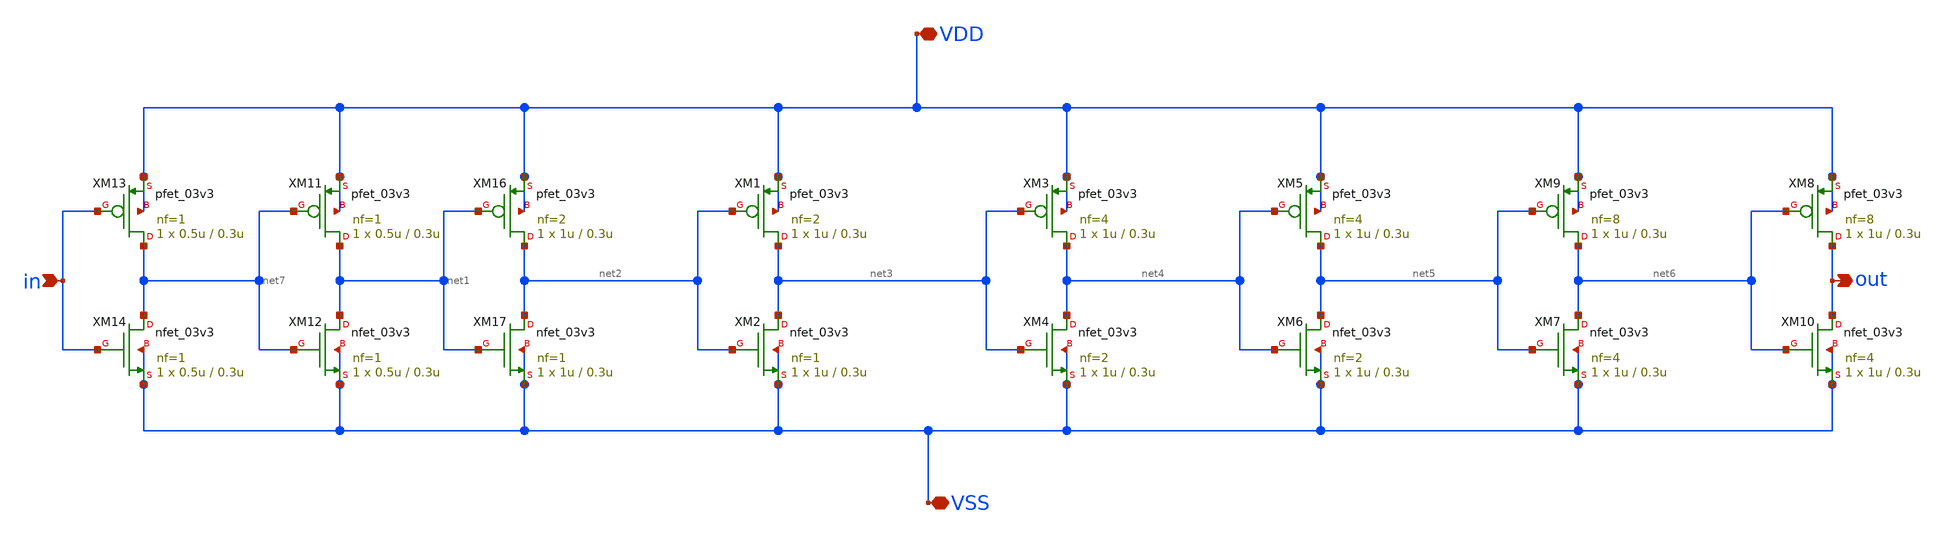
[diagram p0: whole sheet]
** sch_path: designs/libs/core_vco/vco_buffer/vco_buffer.sch
**.subckt vco_buffer in VDD VSS out
*.ipin in
*.iopin VDD
*.iopin VSS
*.opin out
XM16 net2 net1 VDD VDD pfet_03v3 L=0.3u W=1u nf=2 ad='int((nf+1)/2) * W/nf * 0.18u' as='int((nf+2)/2) * W/nf * 0.18u'
+ pd='2*int((nf+1)/2) * (W/nf + 0.18u)' ps='2*int((nf+2)/2) * (W/nf + 0.18u)' nrd='0.18u / W' nrs='0.18u / W'
+ sa=0 sb=0 sd=0 m=1
XM17 net2 net1 VSS VSS nfet_03v3 L=0.3u W=1u nf=1 ad='int((nf+1)/2) * W/nf * 0.18u' as='int((nf+2)/2) * W/nf * 0.18u'
+ pd='2*int((nf+1)/2) * (W/nf + 0.18u)' ps='2*int((nf+2)/2) * (W/nf + 0.18u)' nrd='0.18u / W' nrs='0.18u / W'
+ sa=0 sb=0 sd=0 m=1
XM2 net3 net2 VSS VSS nfet_03v3 L=0.3u W=1u nf=1 ad='int((nf+1)/2) * W/nf * 0.18u' as='int((nf+2)/2) * W/nf * 0.18u'
+ pd='2*int((nf+1)/2) * (W/nf + 0.18u)' ps='2*int((nf+2)/2) * (W/nf + 0.18u)' nrd='0.18u / W' nrs='0.18u / W'
+ sa=0 sb=0 sd=0 m=1
XM4 net4 net3 VSS VSS nfet_03v3 L=0.3u W=1u nf=2 ad='int((nf+1)/2) * W/nf * 0.18u' as='int((nf+2)/2) * W/nf * 0.18u'
+ pd='2*int((nf+1)/2) * (W/nf + 0.18u)' ps='2*int((nf+2)/2) * (W/nf + 0.18u)' nrd='0.18u / W' nrs='0.18u / W'
+ sa=0 sb=0 sd=0 m=1
XM6 net5 net4 VSS VSS nfet_03v3 L=0.3u W=1u nf=2 ad='int((nf+1)/2) * W/nf * 0.18u' as='int((nf+2)/2) * W/nf * 0.18u'
+ pd='2*int((nf+1)/2) * (W/nf + 0.18u)' ps='2*int((nf+2)/2) * (W/nf + 0.18u)' nrd='0.18u / W' nrs='0.18u / W'
+ sa=0 sb=0 sd=0 m=1
XM1 net3 net2 VDD VDD pfet_03v3 L=0.3u W=1u nf=2 ad='int((nf+1)/2) * W/nf * 0.18u' as='int((nf+2)/2) * W/nf * 0.18u'
+ pd='2*int((nf+1)/2) * (W/nf + 0.18u)' ps='2*int((nf+2)/2) * (W/nf + 0.18u)' nrd='0.18u / W' nrs='0.18u / W'
+ sa=0 sb=0 sd=0 m=1
XM3 net4 net3 VDD VDD pfet_03v3 L=0.3u W=1u nf=4 ad='int((nf+1)/2) * W/nf * 0.18u' as='int((nf+2)/2) * W/nf * 0.18u'
+ pd='2*int((nf+1)/2) * (W/nf + 0.18u)' ps='2*int((nf+2)/2) * (W/nf + 0.18u)' nrd='0.18u / W' nrs='0.18u / W'
+ sa=0 sb=0 sd=0 m=1
XM5 net5 net4 VDD VDD pfet_03v3 L=0.3u W=1u nf=4 ad='int((nf+1)/2) * W/nf * 0.18u' as='int((nf+2)/2) * W/nf * 0.18u'
+ pd='2*int((nf+1)/2) * (W/nf + 0.18u)' ps='2*int((nf+2)/2) * (W/nf + 0.18u)' nrd='0.18u / W' nrs='0.18u / W'
+ sa=0 sb=0 sd=0 m=1
XM7 net6 net5 VSS VSS nfet_03v3 L=0.3u W=1u nf=4 ad='int((nf+1)/2) * W/nf * 0.18u' as='int((nf+2)/2) * W/nf * 0.18u'
+ pd='2*int((nf+1)/2) * (W/nf + 0.18u)' ps='2*int((nf+2)/2) * (W/nf + 0.18u)' nrd='0.18u / W' nrs='0.18u / W'
+ sa=0 sb=0 sd=0 m=1
XM9 net6 net5 VDD VDD pfet_03v3 L=0.3u W=1u nf=8 ad='int((nf+1)/2) * W/nf * 0.18u' as='int((nf+2)/2) * W/nf * 0.18u'
+ pd='2*int((nf+1)/2) * (W/nf + 0.18u)' ps='2*int((nf+2)/2) * (W/nf + 0.18u)' nrd='0.18u / W' nrs='0.18u / W'
+ sa=0 sb=0 sd=0 m=1
XM8 out net6 VDD VDD pfet_03v3 L=0.3u W=1u nf=8 ad='int((nf+1)/2) * W/nf * 0.18u' as='int((nf+2)/2) * W/nf * 0.18u'
+ pd='2*int((nf+1)/2) * (W/nf + 0.18u)' ps='2*int((nf+2)/2) * (W/nf + 0.18u)' nrd='0.18u / W' nrs='0.18u / W'
+ sa=0 sb=0 sd=0 m=1
XM10 out net6 VSS VSS nfet_03v3 L=0.3u W=1u nf=4 ad='int((nf+1)/2) * W/nf * 0.18u' as='int((nf+2)/2) * W/nf * 0.18u'
+ pd='2*int((nf+1)/2) * (W/nf + 0.18u)' ps='2*int((nf+2)/2) * (W/nf + 0.18u)' nrd='0.18u / W' nrs='0.18u / W'
+ sa=0 sb=0 sd=0 m=1
XM12 net1 net7 VSS VSS nfet_03v3 L=0.3u W=0.5u nf=1 ad='int((nf+1)/2) * W/nf * 0.18u' as='int((nf+2)/2) * W/nf * 0.18u'
+ pd='2*int((nf+1)/2) * (W/nf + 0.18u)' ps='2*int((nf+2)/2) * (W/nf + 0.18u)' nrd='0.18u / W' nrs='0.18u / W'
+ sa=0 sb=0 sd=0 m=1
XM13 net7 in VDD VDD pfet_03v3 L=0.3u W=0.5u nf=1 ad='int((nf+1)/2) * W/nf * 0.18u' as='int((nf+2)/2) * W/nf * 0.18u'
+ pd='2*int((nf+1)/2) * (W/nf + 0.18u)' ps='2*int((nf+2)/2) * (W/nf + 0.18u)' nrd='0.18u / W' nrs='0.18u / W'
+ sa=0 sb=0 sd=0 m=1
XM14 net7 in VSS VSS nfet_03v3 L=0.3u W=0.5u nf=1 ad='int((nf+1)/2) * W/nf * 0.18u' as='int((nf+2)/2) * W/nf * 0.18u'
+ pd='2*int((nf+1)/2) * (W/nf + 0.18u)' ps='2*int((nf+2)/2) * (W/nf + 0.18u)' nrd='0.18u / W' nrs='0.18u / W'
+ sa=0 sb=0 sd=0 m=1
XM11 net1 net7 VDD VDD pfet_03v3 L=0.3u W=0.5u nf=1 ad='int((nf+1)/2) * W/nf * 0.18u' as='int((nf+2)/2) * W/nf * 0.18u'
+ pd='2*int((nf+1)/2) * (W/nf + 0.18u)' ps='2*int((nf+2)/2) * (W/nf + 0.18u)' nrd='0.18u / W' nrs='0.18u / W'
+ sa=0 sb=0 sd=0 m=1
**.ends
.end
